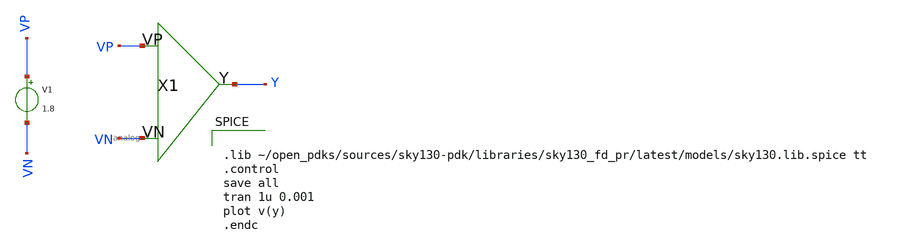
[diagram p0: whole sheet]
** sch_path: Week 3/Week 3/magic_test/xschem/analog_tb.sch
**.subckt analog_tb
X1 analog VP VN Y
V1 VP VN 1.8
**** begin user architecture code


.lib ~/open_pdks/sources/sky130-pdk/libraries/sky130_fd_pr/latest/models/sky130.lib.spice tt
.control
save all
tran 1u 0.001
plot v(y)
.endc

**** end user architecture code
**.ends

* expanding   symbol:  analog.sym # of pins=3
** sym_path: Week 3/Week 3/magic_test/xschem/analog.sym
** sch_path: Week 3/Week 3/magic_test/xschem/analog.sch
.subckt analog
*.iopin VP
*.iopin VN
*.opin Y
XM1 net1 Y VP VP sky130_fd_pr__pfet_01v8 L=0.15 W=1 nf=1 ad='int((nf+1)/2) * W/nf * 0.29' as='int((nf+2)/2) * W/nf * 0.29'
+ pd='2*int((nf+1)/2) * (W/nf + 0.29)' ps='2*int((nf+2)/2) * (W/nf + 0.29)' nrd='0.29 / W' nrs='0.29 / W'
+ sa=0 sb=0 sd=0 mult=1 m=1
XM2 net2 net1 VP VP sky130_fd_pr__pfet_01v8 L=0.15 W=1 nf=1 ad='int((nf+1)/2) * W/nf * 0.29' as='int((nf+2)/2) * W/nf * 0.29'
+ pd='2*int((nf+1)/2) * (W/nf + 0.29)' ps='2*int((nf+2)/2) * (W/nf + 0.29)' nrd='0.29 / W' nrs='0.29 / W'
+ sa=0 sb=0 sd=0 mult=1 m=1
XM3 Y net2 VP VP sky130_fd_pr__pfet_01v8 L=0.15 W=1 nf=1 ad='int((nf+1)/2) * W/nf * 0.29' as='int((nf+2)/2) * W/nf * 0.29'
+ pd='2*int((nf+1)/2) * (W/nf + 0.29)' ps='2*int((nf+2)/2) * (W/nf + 0.29)' nrd='0.29 / W' nrs='0.29 / W'
+ sa=0 sb=0 sd=0 mult=1 m=1
XM4 net1 Y VN VN sky130_fd_pr__nfet_01v8 L=0.15 W=1 nf=1 ad='int((nf+1)/2) * W/nf * 0.29' as='int((nf+2)/2) * W/nf * 0.29'
+ pd='2*int((nf+1)/2) * (W/nf + 0.29)' ps='2*int((nf+2)/2) * (W/nf + 0.29)' nrd='0.29 / W' nrs='0.29 / W'
+ sa=0 sb=0 sd=0 mult=1 m=1
XM5 net2 net1 VN VN sky130_fd_pr__nfet_01v8 L=0.15 W=1 nf=1 ad='int((nf+1)/2) * W/nf * 0.29' as='int((nf+2)/2) * W/nf * 0.29'
+ pd='2*int((nf+1)/2) * (W/nf + 0.29)' ps='2*int((nf+2)/2) * (W/nf + 0.29)' nrd='0.29 / W' nrs='0.29 / W'
+ sa=0 sb=0 sd=0 mult=1 m=1
XM6 Y net2 VN VN sky130_fd_pr__nfet_01v8 L=0.15 W=1 nf=1 ad='int((nf+1)/2) * W/nf * 0.29' as='int((nf+2)/2) * W/nf * 0.29'
+ pd='2*int((nf+1)/2) * (W/nf + 0.29)' ps='2*int((nf+2)/2) * (W/nf + 0.29)' nrd='0.29 / W' nrs='0.29 / W'
+ sa=0 sb=0 sd=0 mult=1 m=1
XC1 net1 VN sky130_fd_pr__cap_mim_m3_1 W=1 L=1 MF=1 m=1
XC2 net2 VN sky130_fd_pr__cap_mim_m3_1 W=1 L=1 MF=1 m=1
XC3 Y VN sky130_fd_pr__cap_mim_m3_1 W=1 L=1 MF=1 m=1
.ends

.end
